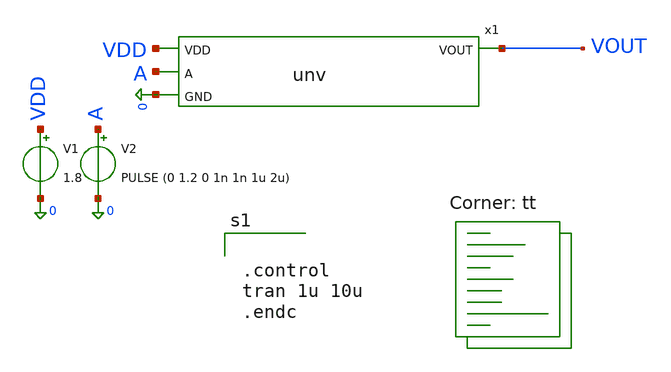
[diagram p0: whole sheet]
** sch_path: inverter/unv_test.sch
**.subckt unv_test
x1 VDD A VOUT 0 unv
V1 VDD 0 1.8
V2 A 0 PULSE (0 1.2 0 1n 1n 1u 2u)
**** begin user architecture code
.lib $::SKYWATER_MODELS/sky130.lib.spice tt


.control
tran 1u 10u
.endc


**** end user architecture code
**.ends

* expanding   symbol:  unv.sym # of pins=4
** sym_path: inverter/unv.sym
** sch_path: inverter/unv.sch
.subckt unv VDD A VOUT GND
*.ipin A
*.ipin VDD
*.ipin GND
*.opin VOUT
XM1 VOUT A VDD VDD sky130_fd_pr__pfet_01v8 L=0.15 W=1 nf=1 ad='int((1 + 1)/2) * 1 / 1 * 0.29' as='int((1 + 2)/2) * 1 / 1 * 0.29'
+ pd='2*int((1 + 1)/2) * (1 / 1 + 0.29)' ps='2*int((1 + 2)/2) * (1 / 1 + 0.29)' nrd='0.29 / 1 ' nrs='0.29 / 1 '
+ sa=0 sb=0 sd=0 mult=1 m=1
XM2 VOUT A GND GND sky130_fd_pr__nfet_01v8 L=0.15 W=1 nf=1 ad='int((1 + 1)/2) * 1 / 1 * 0.29' as='int((1 + 2)/2) * 1 / 1 * 0.29'
+ pd='2*int((1 + 1)/2) * (1 / 1 + 0.29)' ps='2*int((1 + 2)/2) * (1 / 1 + 0.29)' nrd='0.29 / 1 ' nrs='0.29 / 1 '
+ sa=0 sb=0 sd=0 mult=1 m=1
.ends

.end
